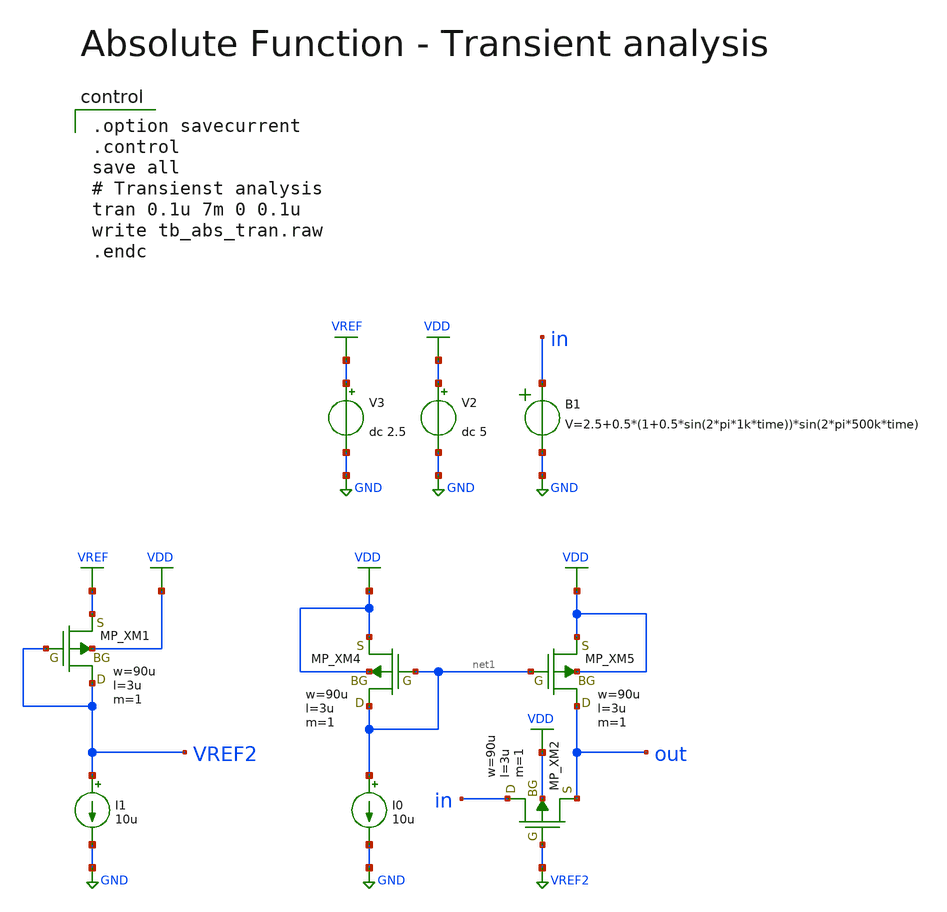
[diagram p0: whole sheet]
** sch_path: member_project/AM_Radio/Yamada3/xschem/tb_abs_tran.sch
**.subckt tb_abs_tran
V2 VDD GND dc 5
I0 net1 GND 10u
V3 VREF GND dc 2.5
XM4 net1 net1 VDD VDD PMOS w=90u l=3u as=0 ad=0 ps=0 pd=0 nrd=0 nrs=0 m=1
XM5 out net1 VDD VDD PMOS w=90u l=3u as=0 ad=0 ps=0 pd=0 nrd=0 nrs=0 m=1
XM2 in VREF2 out VDD PMOS w=90u l=3u as=0 ad=0 ps=0 pd=0 nrd=0 nrs=0 m=1
I1 VREF2 GND 10u
XM1 VREF2 VREF2 VREF VDD PMOS w=90u l=3u as=0 ad=0 ps=0 pd=0 nrd=0 nrs=0 m=1
B1 in GND V=2.5+0.5*(1+0.5*sin(2*pi*1k*time))*sin(2*pi*500k*time)
**** begin user architecture code

.option savecurrent
.control
save all
# Transienst analysis
tran 0.1u 7m 0 0.1u
write tb_abs_tran.raw
.endc

 .include $::LIB/../ip62_models
**** end user architecture code
**.ends
.GLOBAL GND
.GLOBAL VDD
.GLOBAL VREF
.GLOBAL VREF2
.end
